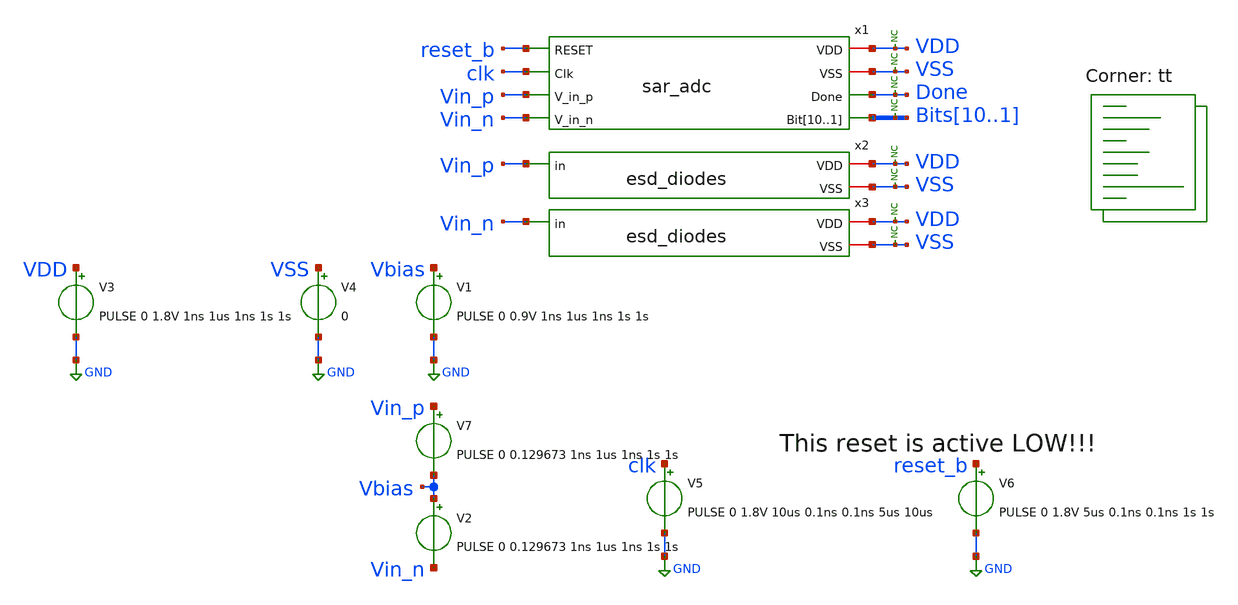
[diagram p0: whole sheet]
** sch_path: xschem/tests/sar_adc/sar_adc_test.sch
**.subckt sar_adc_test
V3 VDD GND PULSE 0 1.8V 1ns 1us 1ns 1s 1s
V4 VSS GND 0
x1 VDD VSS reset_b clk Vin_p Vin_n Done Bits10 Bits9 Bits8 Bits7 Bits6 Bits5 Bits4 Bits3 Bits2 Bits1
+ sar_adc
V2 Vbias Vin_n PULSE 0 0.129673 1ns 1us 1ns 1s 1s
V5 clk GND PULSE 0 1.8V 10us 0.1ns 0.1ns 5us 10us
V6 reset_b GND PULSE 0 1.8V 5us 0.1ns 0.1ns 1s 1s
V1 Vbias GND PULSE 0 0.9V 1ns 1us 1ns 1s 1s
V7 Vin_p Vbias PULSE 0 0.129673 1ns 1us 1ns 1s 1s
* noconn VDD
* noconn VSS
* noconn Done
* noconn Bits[10..1]
* noconn VDD
* noconn VSS
* noconn VDD
* noconn VSS
x2 Vin_p VDD VSS esd_diodes
x3 Vin_n VDD VSS esd_diodes
**** begin user architecture code

*.lib $::SKYWATER_MODELS/sky130.lib.spice tt

* .lib $::SKYWATER_MODELS/sky130.lib.spice.tt.red tt

.include $::SKYWATER_STDCELLS/sky130_fd_sc_hd.spice




.options acct list
.options method=gear
.temp 25
*vvcc VDD 0 dc 1.8
*vvss VSS 0 0
*.ic v(x1.vsampled_p)=0.9V v(x1.vsampled_n)=0.9V
.control
save all
tran 0.1u 340u uic
*plot RST_PLS clk+2 Pulse+4
plot x1.sw_n_sp1 x1.sw_n_sp2+2 x1.sw_n_sp3+4 x1.sw_n_sp4+6 x1.sw_n_sp5+8 x1.sw_n_sp6+10
+ x1.sw_n_sp7+12 x1.sw_n_sp8+14 x1.sw_n_sp9+16
plot x1.sw_p_sp1 x1.sw_p_sp2+2 x1.sw_p_sp3+4 x1.sw_p_sp4+6 x1.sw_p_sp5+8 x1.sw_p_sp6+10
+ x1.sw_p_sp7+12 x1.sw_p_sp8+14 x1.sw_p_sp9+16
plot x1.sw_n1 x1.sw_n2+2 x1.sw_n3+4 x1.sw_n4+6 x1.sw_n5+8 x1.sw_n6+10 x1.sw_n7+12 x1.sw_n8+14
plot x1.sw_p1 x1.sw_p2+2 x1.sw_p3+4 x1.sw_p4+6 x1.sw_p5+8 x1.sw_p6+10 x1.sw_p7+12 x1.sw_p8+14
plot Done-4 Vin_p-Vin_n-2 bits1 bits2+2 bits3+4 bits4+6 bits5+8 bits6+10 bits7+12 bits8+14 bits9+16
+ bits10+18
plot x1.vsampled_p x1.vsampled_n x1.vsampled_p-x1.vsampled_n x1.sw_sample-2 x1.comp_out_p+2
plot x1.vcomp_q x1.comp_out_p x1.x5.net24
plot x1.x1.cycle0 x1.x1.cycle1 x1.x1.cycle2 x1.x1.cycle3 x1.x1.cycle4 x1.x1.cycle5 x1.x1.cycle6
+ x1.x1.cycle7 x1.x1.cycle8 x1.x1.cycle9 x1.x1.cycle10 x1.x1.cycle11 x1.x1.cycle12 x1.x1.cycle13 x1.x1.cycle14
+ x1.x1.cycle15 x1.controller_clk+2
plot x1.comp_out_p-2 x1.comp_out_n-4 x1.x1.raw_bit1 x1.x1.raw_bit2+2 x1.x1.raw_bit3+4
+ x1.x1.raw_bit4+6 x1.x1.raw_bit5+8 x1.x1.raw_bit6+10 x1.x1.raw_bit7+12 x1.x1.raw_bit8+14 x1.x1.raw_bit9+16
+ x1.x1.raw_bit10+18 x1.x1.raw_bit11+20 x1.x1.raw_bit12+22 x1.x1.raw_bit13+24






* write sar_adc_test.raw
.endc* ngspice commands






.lib $::SKYWATER_MODELS/sky130.lib.spice tt
**** end user architecture code
**.ends
.GLOBAL GND
.end
